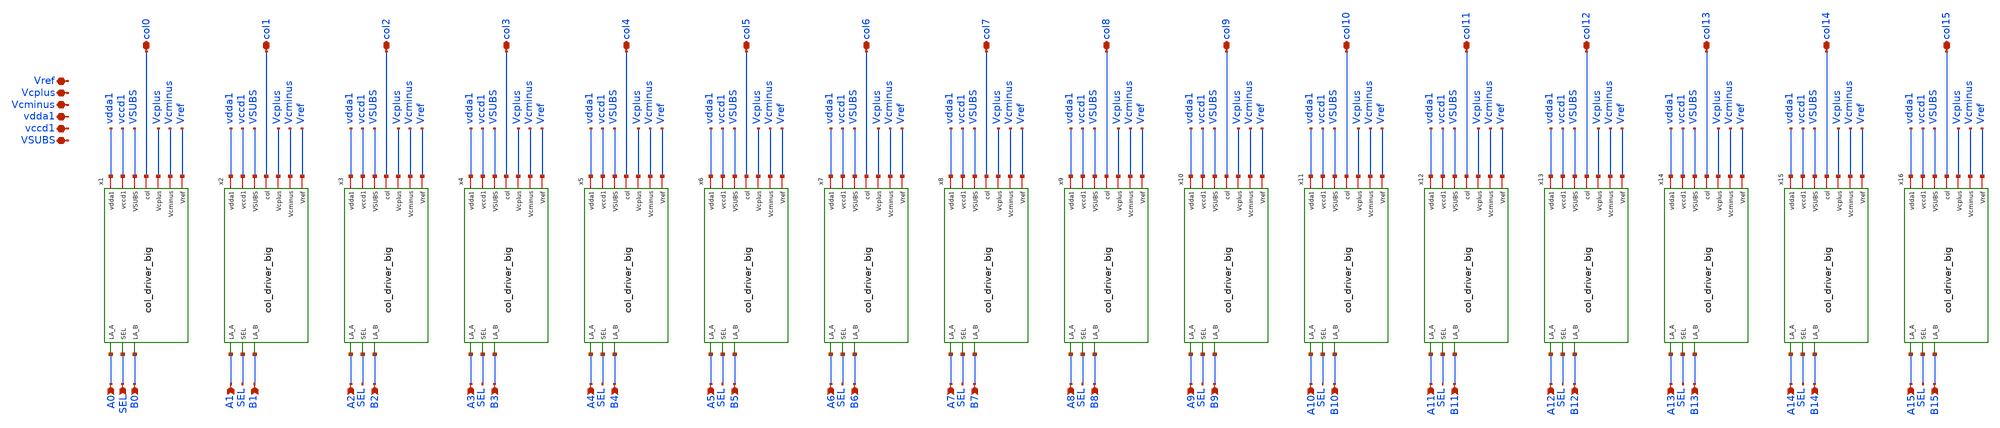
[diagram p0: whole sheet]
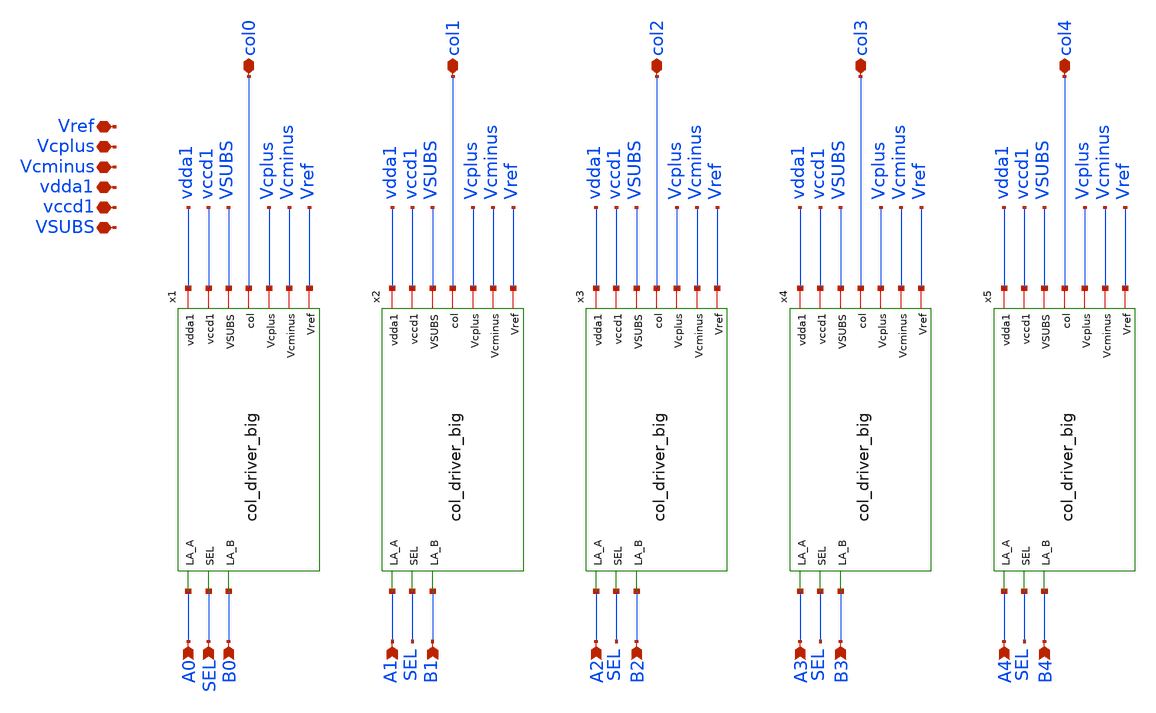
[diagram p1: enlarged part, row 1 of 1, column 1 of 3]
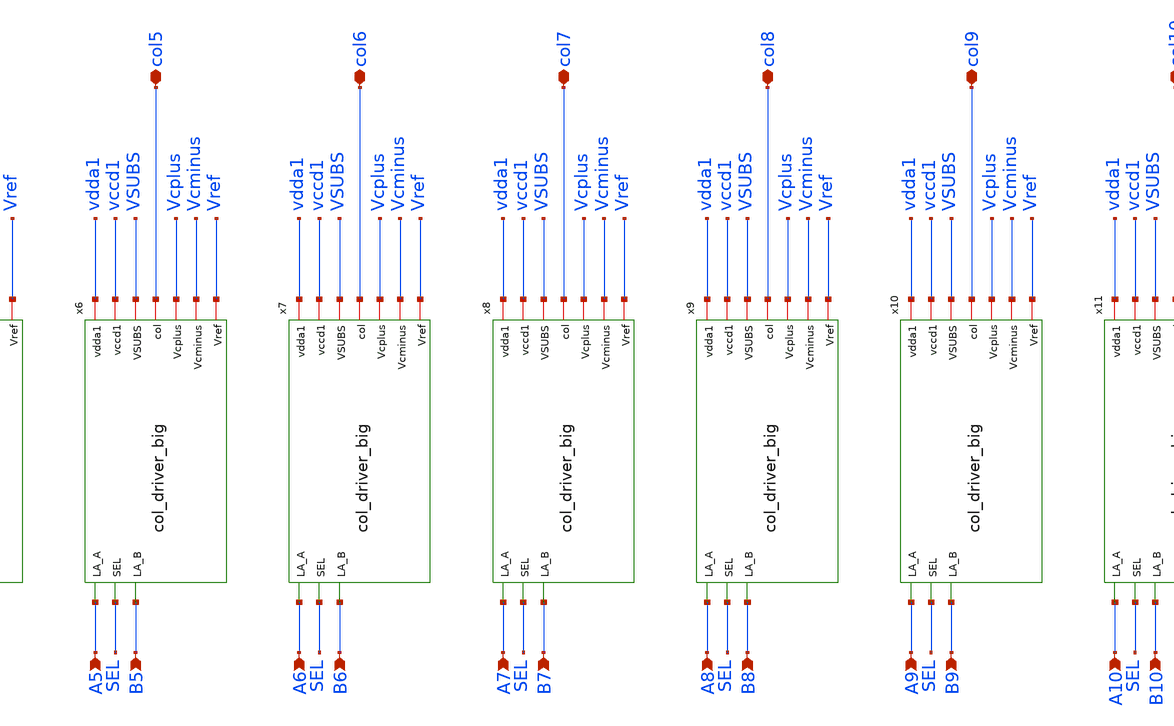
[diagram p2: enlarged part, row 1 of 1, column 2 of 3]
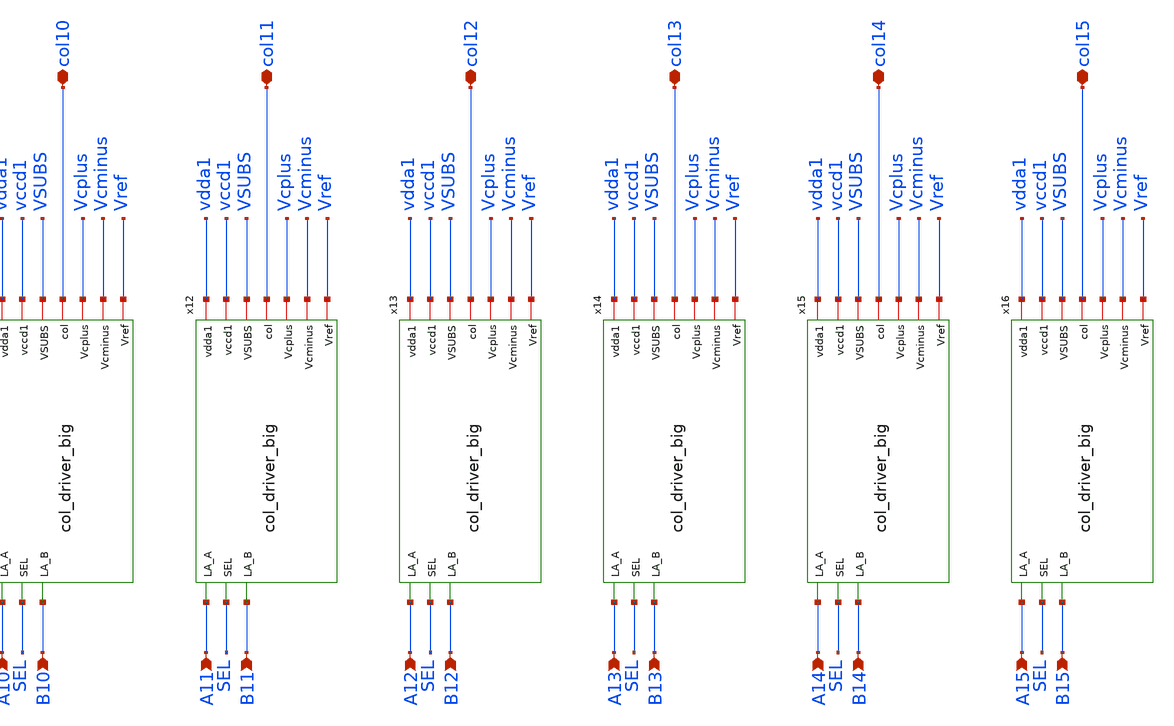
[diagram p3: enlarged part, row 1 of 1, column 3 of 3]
** sch_path: xschem/col_drivers_1x16.sch
**.subckt col_drivers_1x16 vdda1 VSUBS Vref Vcplus Vcminus vccd1 col0 A0 B0 col1 A1 B1 col2 A2 B2
*+ col3 col4 A3 B3 A4 B4 col5 A5 B5 col6 A6 B6 col7 A7 B7 col8 A8 B8 col9 A9 B9 col10 A10 B10 col11 col12
*+ A11 B11 A12 B12 col13 A13 B13 col14 A14 B14 col15 A15 B15 SEL
*.iopin vdda1
*.iopin VSUBS
*.iopin Vref
*.iopin Vcplus
*.iopin Vcminus
*.iopin vccd1
*.iopin col0
*.ipin A0
*.ipin B0
*.iopin col1
*.ipin A1
*.ipin B1
*.iopin col2
*.ipin A2
*.ipin B2
*.iopin col3
*.iopin col4
*.ipin A3
*.ipin B3
*.ipin A4
*.ipin B4
*.iopin col5
*.ipin A5
*.ipin B5
*.iopin col6
*.ipin A6
*.ipin B6
*.iopin col7
*.ipin A7
*.ipin B7
*.iopin col8
*.ipin A8
*.ipin B8
*.iopin col9
*.ipin A9
*.ipin B9
*.iopin col10
*.ipin A10
*.ipin B10
*.iopin col11
*.iopin col12
*.ipin A11
*.ipin B11
*.ipin A12
*.ipin B12
*.iopin col13
*.ipin A13
*.ipin B13
*.iopin col14
*.ipin A14
*.ipin B14
*.iopin col15
*.ipin A15
*.ipin B15
*.ipin SEL
x1 vdda1 vccd1 VSUBS A0 SEL col0 B0 Vcplus Vcminus Vref col_driver_big
x2 vdda1 vccd1 VSUBS A1 SEL col1 B1 Vcplus Vcminus Vref col_driver_big
x3 vdda1 vccd1 VSUBS A2 SEL col2 B2 Vcplus Vcminus Vref col_driver_big
x4 vdda1 vccd1 VSUBS A3 SEL col3 B3 Vcplus Vcminus Vref col_driver_big
x5 vdda1 vccd1 VSUBS A4 SEL col4 B4 Vcplus Vcminus Vref col_driver_big
x6 vdda1 vccd1 VSUBS A5 SEL col5 B5 Vcplus Vcminus Vref col_driver_big
x7 vdda1 vccd1 VSUBS A6 SEL col6 B6 Vcplus Vcminus Vref col_driver_big
x8 vdda1 vccd1 VSUBS A7 SEL col7 B7 Vcplus Vcminus Vref col_driver_big
x9 vdda1 vccd1 VSUBS A8 SEL col8 B8 Vcplus Vcminus Vref col_driver_big
x10 vdda1 vccd1 VSUBS A9 SEL col9 B9 Vcplus Vcminus Vref col_driver_big
x11 vdda1 vccd1 VSUBS A10 SEL col10 B10 Vcplus Vcminus Vref col_driver_big
x12 vdda1 vccd1 VSUBS A11 SEL col11 B11 Vcplus Vcminus Vref col_driver_big
x13 vdda1 vccd1 VSUBS A12 SEL col12 B12 Vcplus Vcminus Vref col_driver_big
x14 vdda1 vccd1 VSUBS A13 SEL col13 B13 Vcplus Vcminus Vref col_driver_big
x15 vdda1 vccd1 VSUBS A14 SEL col14 B14 Vcplus Vcminus Vref col_driver_big
x16 vdda1 vccd1 VSUBS A15 SEL col15 B15 Vcplus Vcminus Vref col_driver_big
**.ends
.end
